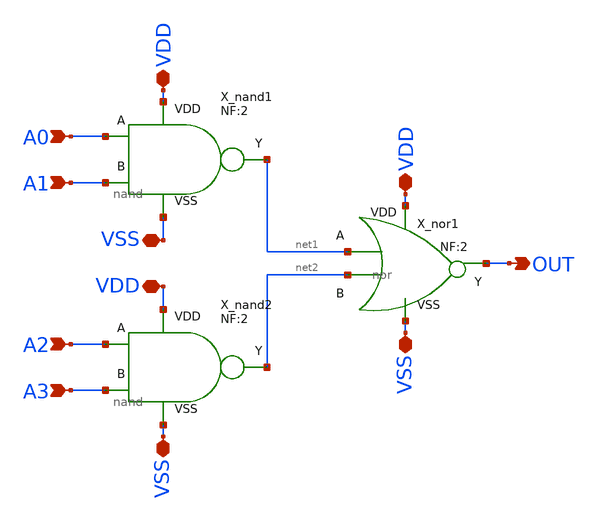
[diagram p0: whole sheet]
** sch_path: xschem_lib/DFFRAM_full_custom/and_4in.sch
**.subckt and_4in VDD VDD VSS VSS VSS VDD A0 A1 A2 A3 OUT
*.iopin VDD
*.iopin VDD
*.iopin VSS
*.iopin VSS
*.iopin VSS
*.iopin VDD
*.ipin A0
*.ipin A1
*.ipin A2
*.ipin A3
*.opin OUT
X_nand1 A1 A0 net1 VDD VSS nand NF=2
X_nand2 A3 A2 net2 VDD VSS nand NF=2
X_nor1 OUT net1 net2 VDD VSS nor NF=2
**.ends

* expanding   symbol:  xschem_lib/DFFRAM_full_custom/nand.sym # of pins=5
** sym_path: xschem_lib/sylee21/nand.sym
** sch_path: xschem_lib/sylee21/nand.sch
.subckt nand B A Y VDD VSS  NF=2
*.opin Y
*.ipin A
*.iopin VDD
*.iopin VSS
*.ipin B
XM1 Y A net1 VSS sky130_fd_pr__nfet_01v8_lvt L=0.15 W=1.2 nf=1 ad='int((nf+1)/2) * W/nf * 0.29' as='int((nf+2)/2) * W/nf * 0.29'
+ pd='2*int((nf+1)/2) * (W/nf + 0.29)' ps='2*int((nf+2)/2) * (W/nf + 0.29)' nrd='0.29 / W' nrs='0.29 / W'
+ sa=0 sb=0 sd=0 mult=NF m=NF
XM2 net1 B VSS VSS sky130_fd_pr__nfet_01v8_lvt L=0.15 W=1.2 nf=1 ad='int((nf+1)/2) * W/nf * 0.29' as='int((nf+2)/2) * W/nf * 0.29'
+ pd='2*int((nf+1)/2) * (W/nf + 0.29)' ps='2*int((nf+2)/2) * (W/nf + 0.29)' nrd='0.29 / W' nrs='0.29 / W'
+ sa=0 sb=0 sd=0 mult=NF m=NF
XM3 Y B VDD VDD sky130_fd_pr__pfet_01v8 L=0.15 W=2.4 nf=1 ad='int((nf+1)/2) * W/nf * 0.29' as='int((nf+2)/2) * W/nf * 0.29'
+ pd='2*int((nf+1)/2) * (W/nf + 0.29)' ps='2*int((nf+2)/2) * (W/nf + 0.29)' nrd='0.29 / W' nrs='0.29 / W'
+ sa=0 sb=0 sd=0 mult=NF m=NF
XM4 Y A VDD VDD sky130_fd_pr__pfet_01v8 L=0.15 W=2.4 nf=1 ad='int((nf+1)/2) * W/nf * 0.29' as='int((nf+2)/2) * W/nf * 0.29'
+ pd='2*int((nf+1)/2) * (W/nf + 0.29)' ps='2*int((nf+2)/2) * (W/nf + 0.29)' nrd='0.29 / W' nrs='0.29 / W'
+ sa=0 sb=0 sd=0 mult=NF m=NF
.ends


* expanding   symbol:  xschem_lib/DFFRAM_full_custom/nor.sym # of pins=5
** sym_path: xschem_lib/DFFRAM_full_custom/nor.sym
** sch_path: xschem_lib/DFFRAM_full_custom/nor.sch
.subckt nor Y A B VDD VSS  NF=2
*.iopin VDD
*.iopin VSS
*.opin Y
*.ipin A
*.ipin B
XM1 Y B VSS VSS sky130_fd_pr__nfet_01v8_lvt L=0.15 W=NF*1.2 nf=NF ad='int((nf+1)/2) * W/nf * 0.29' as='int((nf+2)/2) * W/nf * 0.29'
+ pd='2*int((nf+1)/2) * (W/nf + 0.29)' ps='2*int((nf+2)/2) * (W/nf + 0.29)' nrd='0.29 / W' nrs='0.29 / W'
+ sa=0 sb=0 sd=0 mult=1 m=1
XM4 net1 B VDD VDD sky130_fd_pr__pfet_01v8 L=0.15 W=NF*2.4 nf=NF ad='int((nf+1)/2) * W/nf * 0.29' as='int((nf+2)/2) * W/nf * 0.29'
+ pd='2*int((nf+1)/2) * (W/nf + 0.29)' ps='2*int((nf+2)/2) * (W/nf + 0.29)' nrd='0.29 / W' nrs='0.29 / W'
+ sa=0 sb=0 sd=0 mult=1 m=1
XM3 Y A net1 VDD sky130_fd_pr__pfet_01v8 L=0.15 W=NF*2.4 nf=NF ad='int((nf+1)/2) * W/nf * 0.29' as='int((nf+2)/2) * W/nf * 0.29'
+ pd='2*int((nf+1)/2) * (W/nf + 0.29)' ps='2*int((nf+2)/2) * (W/nf + 0.29)' nrd='0.29 / W' nrs='0.29 / W'
+ sa=0 sb=0 sd=0 mult=1 m=1
XM2 Y A VSS VSS sky130_fd_pr__nfet_01v8_lvt L=0.15 W=NF*1.2 nf=NF ad='int((nf+1)/2) * W/nf * 0.29' as='int((nf+2)/2) * W/nf * 0.29'
+ pd='2*int((nf+1)/2) * (W/nf + 0.29)' ps='2*int((nf+2)/2) * (W/nf + 0.29)' nrd='0.29 / W' nrs='0.29 / W'
+ sa=0 sb=0 sd=0 mult=1 m=1
.ends

.end
